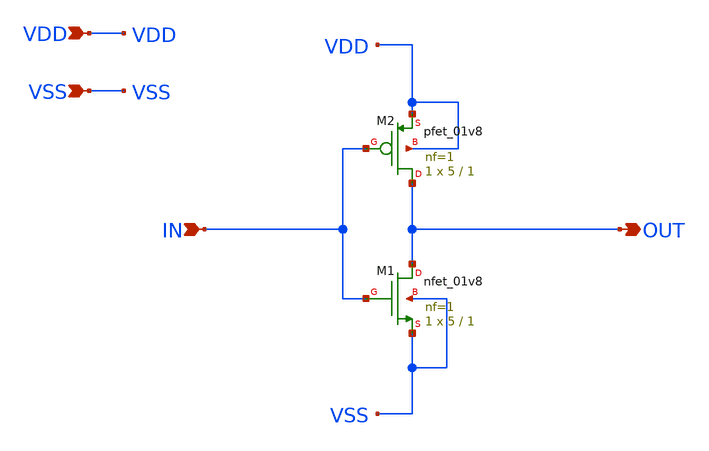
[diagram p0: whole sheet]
** sch_path: custom_gds/tt_um_alexjaeger_ringoscillator/xschem/notbig.sch
**.subckt notbig OUT IN VDD VSS
*.opin OUT
*.ipin IN
*.ipin VDD
*.ipin VSS
XM1 OUT IN VSS VSS sky130_fd_pr__nfet_01v8 L=1 W=5 nf=1 ad='int((nf+1)/2) * W/nf * 0.29' as='int((nf+2)/2) * W/nf * 0.29'
+ pd='2*int((nf+1)/2) * (W/nf + 0.29)' ps='2*int((nf+2)/2) * (W/nf + 0.29)' nrd='0.29 / W' nrs='0.29 / W'
+ sa=0 sb=0 sd=0 mult=1 m=1
XM2 OUT IN VDD VDD sky130_fd_pr__pfet_01v8 L=1 W=5 nf=1 ad='int((nf+1)/2) * W/nf * 0.29' as='int((nf+2)/2) * W/nf * 0.29'
+ pd='2*int((nf+1)/2) * (W/nf + 0.29)' ps='2*int((nf+2)/2) * (W/nf + 0.29)' nrd='0.29 / W' nrs='0.29 / W'
+ sa=0 sb=0 sd=0 mult=1 m=1
**.ends
.end
